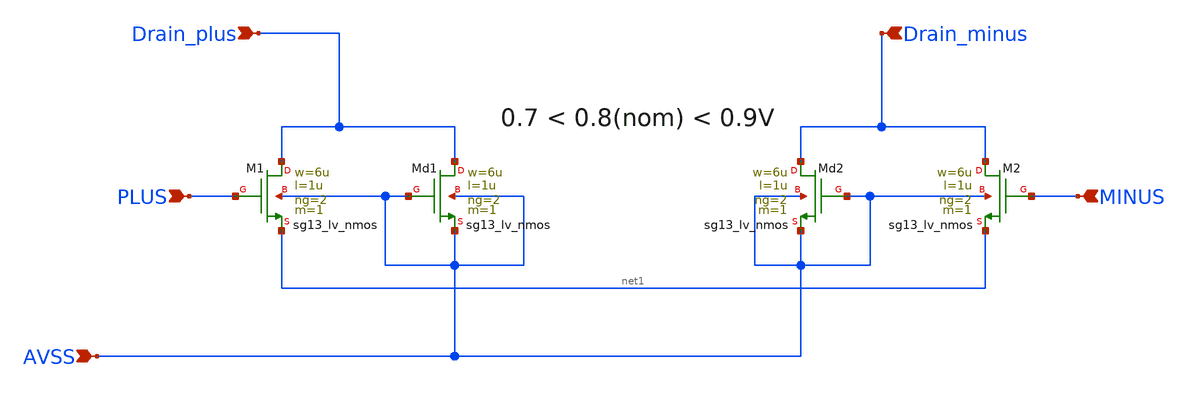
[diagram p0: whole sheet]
** sch_path: Designs/otas/1_schematics/diff_pair.sch
**.subckt diff_pair PLUS MINUS AVSS Drain_plus Drain_minus
*.ipin PLUS
*.ipin MINUS
*.ipin AVSS
*.ipin Drain_plus
*.ipin Drain_minus
XM1 Drain_plus PLUS net1 AVSS sg13_lv_nmos w=6u l=1u ng=2 m=1 mm_ok=1
XM2 Drain_minus MINUS net1 AVSS sg13_lv_nmos w=6u l=1u ng=2 m=1 mm_ok=1
XMd2 Drain_minus AVSS AVSS AVSS sg13_lv_nmos w=6u l=1u ng=2 m=1 mm_ok=1
XMd1 Drain_plus AVSS AVSS AVSS sg13_lv_nmos w=6u l=1u ng=2 m=1 mm_ok=1
**.ends
.end
